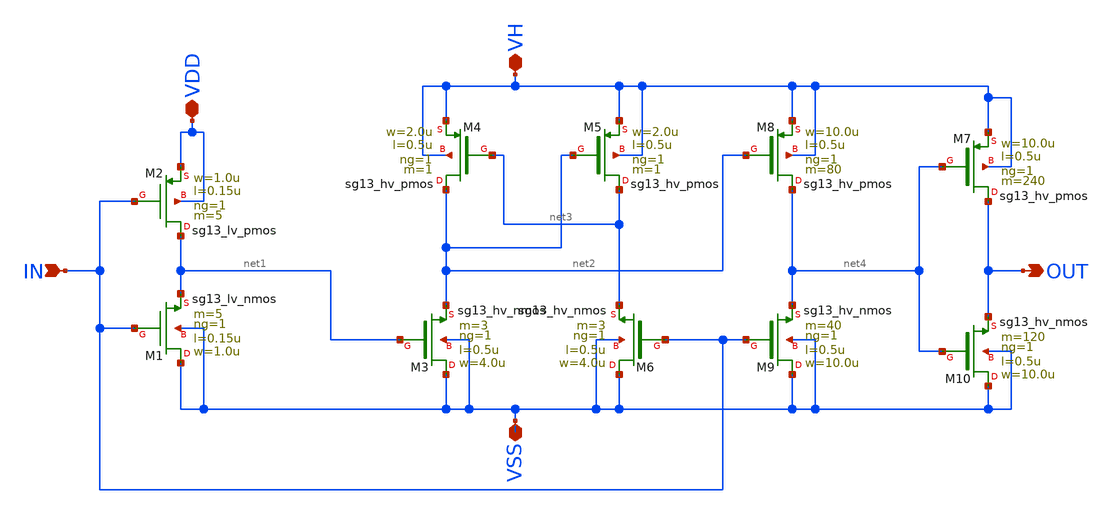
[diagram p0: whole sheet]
** sch_path: xschem/LS_FINAL_IHP_v3p1.sch
**.subckt LS_FINAL_IHP_v3p1 IN VDD VH OUT VSS
*.ipin IN
*.iopin VDD
*.iopin VH
*.opin OUT
*.iopin VSS
XM1 VSS IN net1 VSS sg13_lv_nmos w=1.0u l=0.15u ng=1 m=5 mm_ok=1
XM2 net1 IN VDD VDD sg13_lv_pmos w=1.0u l=0.15u ng=1 m=5 mm_ok=1
XM3 VSS net1 net2 VSS sg13_hv_nmos w=4.0u l=0.5u ng=1 m=3 mm_ok=1
XM4 net2 net3 VH VH sg13_hv_pmos w=2.0u l=0.5u ng=1 m=1 mm_ok=1
XM5 net3 net2 VH VH sg13_hv_pmos w=2.0u l=0.5u ng=1 m=1 mm_ok=1
XM6 VSS IN net3 VSS sg13_hv_nmos w=4.0u l=0.5u ng=1 m=3 mm_ok=1
XM8 net4 net2 VH VH sg13_hv_pmos w=10.0u l=0.5u ng=1 m=80 mm_ok=1
XM9 VSS IN net4 VSS sg13_hv_nmos w=10.0u l=0.5u ng=1 m=40 mm_ok=1
XM7 OUT net4 VH VH sg13_hv_pmos w=10.0u l=0.5u ng=1 m=240 mm_ok=1
XM10 VSS net4 OUT VSS sg13_hv_nmos w=10.0u l=0.5u ng=1 m=120 mm_ok=1
**.ends
.end
